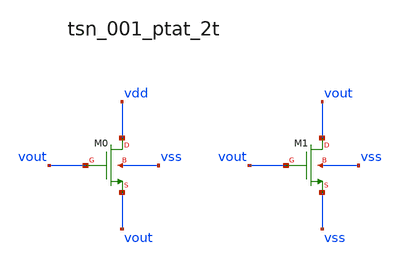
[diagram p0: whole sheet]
** sch_path: analog-db/raw/tsn_001_ptat_2t/hier/tsn_001_ptat_2t.sch
**.subckt tsn_001_ptat_2t
XM0 vdd vout vout vss sg13_lv_nmos w=x_dut_xm0_w l=x_dut_xm0_l ng=1 m=x_dut_xm0_m
XM1 vout vout vss vss sg13_lv_nmos w=x_dut_xm1_w l=x_dut_xm1_l ng=1 m=x_dut_xm1_m
**.ends
.end
